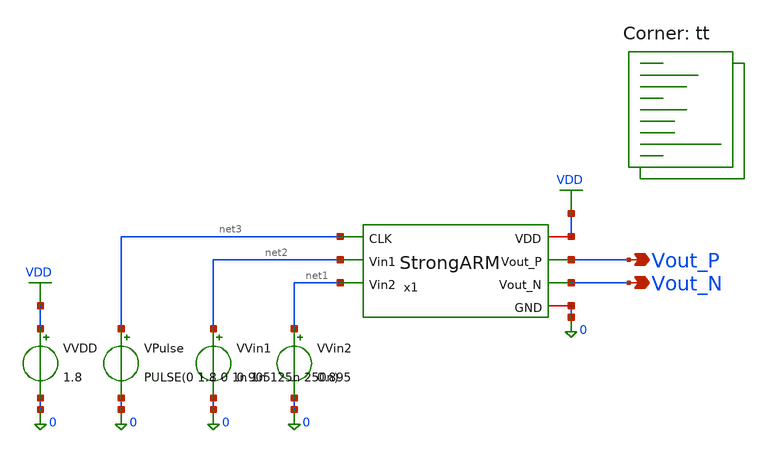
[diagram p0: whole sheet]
** sch_path: blocks/03_StrongARM/sim/tb_StrongARM_Transient.sch
**.subckt tb_StrongARM_Transient Vout_P Vout_N
*.opin Vout_P
*.opin Vout_N
x1 VDD net3 Vout_P Vout_N net2 net1 0 StrongARM
VVDD VDD 0 1.8
VVin1 net2 0 0.905
VVin2 net1 0 0.895
VPulse net3 0 PULSE(0 1.8 0 1n 1n 125n 250n)
**** begin user architecture code


.control
save all
tran 0.2n 3u

plot v(CLK)
plot v(Vin1) v(Vin2)
plot v(Vout_P) v(Vout_N)

.endc


.lib $::SKYWATER_MODELS/sky130.lib.spice tt
**** end user architecture code
**.ends

* expanding   symbol:  blocks/03_StrongARM/xschem/StrongARM.sym # of pins=7
** sym_path: blocks/03_StrongARM/xschem/StrongARM.sym
** sch_path: blocks/03_StrongARM/xschem/StrongARM.sch
.subckt StrongARM VDD CLK Vout_P Vout_N Vin1 Vin2 GND
*.iopin VDD
*.iopin GND
*.ipin Vin1
*.ipin Vin2
*.ipin CLK
*.opin Vout_P
*.opin Vout_N
XS1 P CLK VDD VDD sky130_fd_pr__pfet_01v8 L=0.15 W=1.5 nf=1 ad='int((1 + 1)/2) * 1.5 / 1 * 0.29' as='int((1 + 2)/2) * 1.5 / 1 * 0.29'
+ pd='2*int((1 + 1)/2) * (1.5 / 1 + 0.29)' ps='2*int((1 + 2)/2) * (1.5 / 1 + 0.29)' nrd='0.29 / 1.5 ' nrs='0.29 / 1.5 '
+ sa=0 sb=0 sd=0 mult=1 m=1
XS3 Vout_P CLK VDD VDD sky130_fd_pr__pfet_01v8 L=0.15 W=1.5 nf=1 ad='int((1 + 1)/2) * 1.5 / 1 * 0.29'
+ as='int((1 + 2)/2) * 1.5 / 1 * 0.29' pd='2*int((1 + 1)/2) * (1.5 / 1 + 0.29)' ps='2*int((1 + 2)/2) * (1.5 / 1 + 0.29)'
+ nrd='0.29 / 1.5 ' nrs='0.29 / 1.5 ' sa=0 sb=0 sd=0 mult=1 m=1
XM5 Vout_P Vout_N VDD VDD sky130_fd_pr__pfet_01v8 L=0.3 W=5 nf=1 ad='int((1 + 1)/2) * 5 / 1 * 0.29' as='int((1 + 2)/2) * 5 / 1 * 0.29'
+ pd='2*int((1 + 1)/2) * (5 / 1 + 0.29)' ps='2*int((1 + 2)/2) * (5 / 1 + 0.29)' nrd='0.29 / 5 ' nrs='0.29 / 5 '
+ sa=0 sb=0 sd=0 mult=1 m=1
XM6 Vout_N Vout_P VDD VDD sky130_fd_pr__pfet_01v8 L=0.3 W=5 nf=1 ad='int((1 + 1)/2) * 5 / 1 * 0.29' as='int((1 + 2)/2) * 5 / 1 * 0.29'
+ pd='2*int((1 + 1)/2) * (5 / 1 + 0.29)' ps='2*int((1 + 2)/2) * (5 / 1 + 0.29)' nrd='0.29 / 5 ' nrs='0.29 / 5 '
+ sa=0 sb=0 sd=0 mult=1 m=1
XS4 Vout_N CLK VDD VDD sky130_fd_pr__pfet_01v8 L=0.15 W=1.5 nf=1 ad='int((1 + 1)/2) * 1.5 / 1 * 0.29'
+ as='int((1 + 2)/2) * 1.5 / 1 * 0.29' pd='2*int((1 + 1)/2) * (1.5 / 1 + 0.29)' ps='2*int((1 + 2)/2) * (1.5 / 1 + 0.29)'
+ nrd='0.29 / 1.5 ' nrs='0.29 / 1.5 ' sa=0 sb=0 sd=0 mult=1 m=1
XS2 Q CLK VDD VDD sky130_fd_pr__pfet_01v8 L=0.15 W=1.5 nf=1 ad='int((1 + 1)/2) * 1.5 / 1 * 0.29' as='int((1 + 2)/2) * 1.5 / 1 * 0.29'
+ pd='2*int((1 + 1)/2) * (1.5 / 1 + 0.29)' ps='2*int((1 + 2)/2) * (1.5 / 1 + 0.29)' nrd='0.29 / 1.5 ' nrs='0.29 / 1.5 '
+ sa=0 sb=0 sd=0 mult=1 m=1
XM3 Vout_P Vout_N P GND sky130_fd_pr__nfet_01v8 L=0.3 W=2 nf=1 ad='int((1 + 1)/2) * 2 / 1 * 0.29' as='int((1 + 2)/2) * 2 / 1 * 0.29'
+ pd='2*int((1 + 1)/2) * (2 / 1 + 0.29)' ps='2*int((1 + 2)/2) * (2 / 1 + 0.29)' nrd='0.29 / 2 ' nrs='0.29 / 2 '
+ sa=0 sb=0 sd=0 mult=1 m=1
XM4 Vout_N Vout_P Q GND sky130_fd_pr__nfet_01v8 L=0.3 W=2 nf=1 ad='int((1 + 1)/2) * 2 / 1 * 0.29' as='int((1 + 2)/2) * 2 / 1 * 0.29'
+ pd='2*int((1 + 1)/2) * (2 / 1 + 0.29)' ps='2*int((1 + 2)/2) * (2 / 1 + 0.29)' nrd='0.29 / 2 ' nrs='0.29 / 2 '
+ sa=0 sb=0 sd=0 mult=1 m=1
XM1 P Vin1 TAIL GND sky130_fd_pr__nfet_01v8 L=0.5 W=10 nf=1 ad='int((1 + 1)/2) * 10 / 1 * 0.29' as='int((1 + 2)/2) * 10 / 1 * 0.29'
+ pd='2*int((1 + 1)/2) * (10 / 1 + 0.29)' ps='2*int((1 + 2)/2) * (10 / 1 + 0.29)' nrd='0.29 / 10 ' nrs='0.29 / 10 '
+ sa=0 sb=0 sd=0 mult=1 m=1
XM2 Q Vin2 TAIL GND sky130_fd_pr__nfet_01v8 L=0.5 W=10 nf=1 ad='int((1 + 1)/2) * 10 / 1 * 0.29' as='int((1 + 2)/2) * 10 / 1 * 0.29'
+ pd='2*int((1 + 1)/2) * (10 / 1 + 0.29)' ps='2*int((1 + 2)/2) * (10 / 1 + 0.29)' nrd='0.29 / 10 ' nrs='0.29 / 10 '
+ sa=0 sb=0 sd=0 mult=1 m=1
XM7 TAIL CLK GND GND sky130_fd_pr__nfet_01v8 L=0.3 W=1 nf=1 ad='int((1 + 1)/2) * 1 / 1 * 0.29' as='int((1 + 2)/2) * 1 / 1 * 0.29'
+ pd='2*int((1 + 1)/2) * (1 / 1 + 0.29)' ps='2*int((1 + 2)/2) * (1 / 1 + 0.29)' nrd='0.29 / 1 ' nrs='0.29 / 1 '
+ sa=0 sb=0 sd=0 mult=1 m=1
.ends

.GLOBAL VDD
.end
